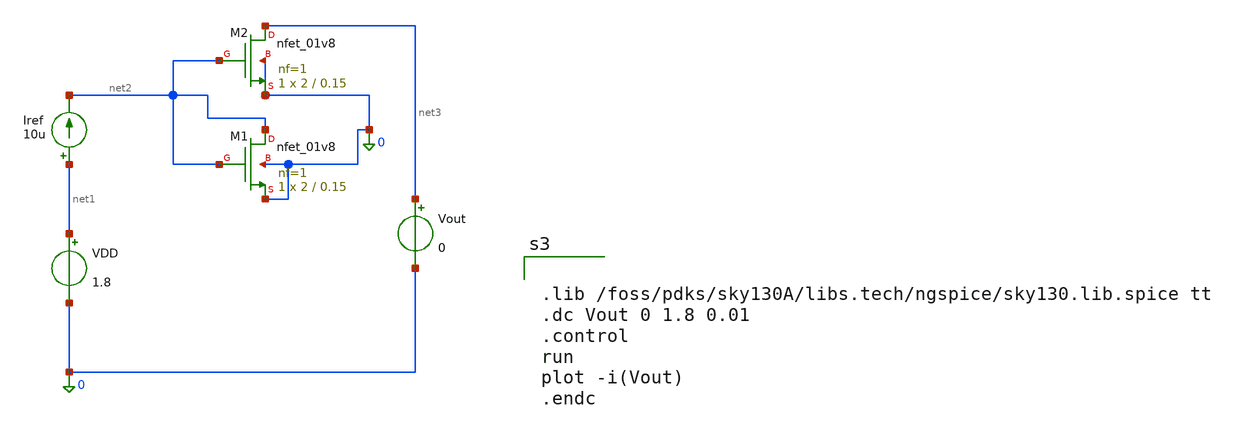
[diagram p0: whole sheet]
** sch_path: week2_current_mirror/simulations/current_mirror_tb_L015.sch
**.subckt current_mirror_tb_L015
XM2 net3 net2 0 0 sky130_fd_pr__nfet_01v8 L=0.15 W=2 nf=1 ad='int((1 + 1)/2) * 2 / 1 * 0.29' as='int((1 + 2)/2) * 2 / 1 * 0.29'
+ pd='2*int((1 + 1)/2) * (2 / 1 + 0.29)' ps='2*int((1 + 2)/2) * (2 / 1 + 0.29)' nrd='0.29 / 2 ' nrs='0.29 / 2 '
+ sa=0 sb=0 sd=0 mult=1 m=1
Vout net3 0 0
XM1 net2 net2 0 0 sky130_fd_pr__nfet_01v8 L=0.15 W=2 nf=1 ad='int((1 + 1)/2) * 2 / 1 * 0.29' as='int((1 + 2)/2) * 2 / 1 * 0.29'
+ pd='2*int((1 + 1)/2) * (2 / 1 + 0.29)' ps='2*int((1 + 2)/2) * (2 / 1 + 0.29)' nrd='0.29 / 2 ' nrs='0.29 / 2 '
+ sa=0 sb=0 sd=0 mult=1 m=1
Iref net1 net2 10u
VDD net1 0 1.8
**** begin user architecture code


.lib /foss/pdks/sky130A/libs.tech/ngspice/sky130.lib.spice tt
.dc Vout 0 1.8 0.01
.control
run
plot -i(Vout)
.endc


**** end user architecture code
**.ends
.end
